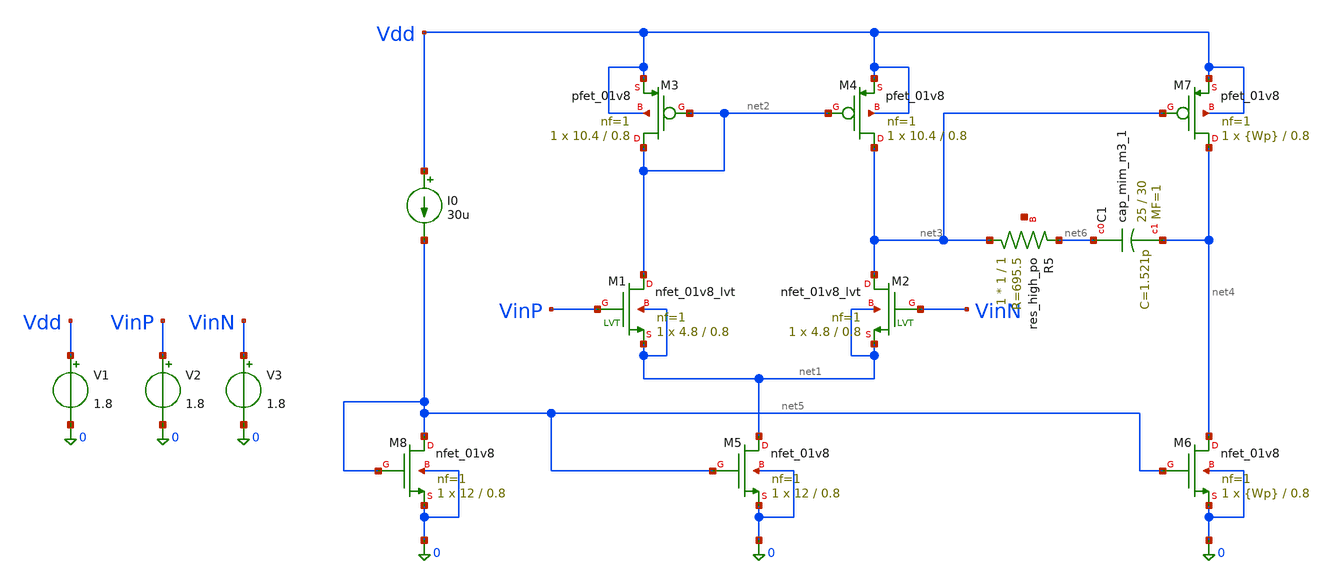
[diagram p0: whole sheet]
** sch_path: parameter_extraction/opamp.sch
**.subckt opamp
XM1 net2 VinP net1 net1 sky130_fd_pr__nfet_01v8_lvt L=0.8 W=4.8 nf=1 ad='int((1 + 1)/2) * 4.8 / 1 * 0.29'
+ as='int((1 + 2)/2) * 4.8 / 1 * 0.29' pd='2*int((1 + 1)/2) * (4.8 / 1 + 0.29)' ps='2*int((1 + 2)/2) * (4.8 / 1 + 0.29)'
+ nrd='0.29 / 4.8 ' nrs='0.29 / 4.8 ' sa=0 sb=0 sd=0 mult=1 m=1
XM3 net2 net2 Vdd Vdd sky130_fd_pr__pfet_01v8 L=0.8 W=10.4 nf=1 ad='int((1 + 1)/2) * 10.4 / 1 * 0.29'
+ as='int((1 + 2)/2) * 10.4 / 1 * 0.29' pd='2*int((1 + 1)/2) * (10.4 / 1 + 0.29)' ps='2*int((1 + 2)/2) * (10.4 / 1 + 0.29)'
+ nrd='0.29 / 10.4 ' nrs='0.29 / 10.4 ' sa=0 sb=0 sd=0 mult=1 m=1
XM5 net1 net5 0 0 sky130_fd_pr__nfet_01v8 L=0.8 W=12 nf=1 ad='int((1 + 1)/2) * 12 / 1 * 0.29' as='int((1 + 2)/2) * 12 / 1 * 0.29'
+ pd='2*int((1 + 1)/2) * (12 / 1 + 0.29)' ps='2*int((1 + 2)/2) * (12 / 1 + 0.29)' nrd='0.29 / 12 ' nrs='0.29 / 12 '
+ sa=0 sb=0 sd=0 mult=1 m=1
XM2 net3 VinN net1 net1 sky130_fd_pr__nfet_01v8_lvt L=0.8 W=4.8 nf=1 ad='int((1 + 1)/2) * 4.8 / 1 * 0.29'
+ as='int((1 + 2)/2) * 4.8 / 1 * 0.29' pd='2*int((1 + 1)/2) * (4.8 / 1 + 0.29)' ps='2*int((1 + 2)/2) * (4.8 / 1 + 0.29)'
+ nrd='0.29 / 4.8 ' nrs='0.29 / 4.8 ' sa=0 sb=0 sd=0 mult=1 m=1
XM4 net3 net2 Vdd Vdd sky130_fd_pr__pfet_01v8 L=0.8 W=10.4 nf=1 ad='int((1 + 1)/2) * 10.4 / 1 * 0.29'
+ as='int((1 + 2)/2) * 10.4 / 1 * 0.29' pd='2*int((1 + 1)/2) * (10.4 / 1 + 0.29)' ps='2*int((1 + 2)/2) * (10.4 / 1 + 0.29)'
+ nrd='0.29 / 10.4 ' nrs='0.29 / 10.4 ' sa=0 sb=0 sd=0 mult=1 m=1
XM6 net4 net5 0 0 sky130_fd_pr__nfet_01v8 L=0.8 W={Wp} nf=1 ad='int((1 + 1)/2) * {Wp} / 1 * 0.29' as='int((1 + 2)/2) * {Wp} / 1 * 0.29'
+ pd='2*int((1 + 1)/2) * ({Wp} / 1 + 0.29)' ps='2*int((1 + 2)/2) * ({Wp} / 1 + 0.29)' nrd='0.29 / {Wp} '
+ nrs='0.29 / {Wp} ' sa=0 sb=0 sd=0 mult=1 m=1
XM7 net4 net3 Vdd Vdd sky130_fd_pr__pfet_01v8 L=0.8 W={Wp} nf=1 ad='int((1 + 1)/2) * {Wp} / 1 * 0.29'
+ as='int((1 + 2)/2) * {Wp} / 1 * 0.29' pd='2*int((1 + 1)/2) * ({Wp} / 1 + 0.29)' ps='2*int((1 + 2)/2) * ({Wp} / 1 + 0.29)'
+ nrd='0.29 / {Wp} ' nrs='0.29 / {Wp} ' sa=0 sb=0 sd=0 mult=1 m=1
XC1 net6 net4 sky130_fd_pr__cap_mim_m3_1 W=25 L=30 MF=1 m=1
XM8 net5 net5 0 0 sky130_fd_pr__nfet_01v8 L=0.8 W=12 nf=1 ad='int((1 + 1)/2) * 12 / 1 * 0.29' as='int((1 + 2)/2) * 12 / 1 * 0.29'
+ pd='2*int((1 + 1)/2) * (12 / 1 + 0.29)' ps='2*int((1 + 2)/2) * (12 / 1 + 0.29)' nrd='0.29 / 12 ' nrs='0.29 / 12 '
+ sa=0 sb=0 sd=0 mult=1 m=1
V1 Vdd 0 1.8
I0 Vdd net5 30u
V2 VinP 0 1.8
V3 VinN 0 1.8
XR5 net3 net6 net7 sky130_fd_pr__res_high_po W=1 L=1 mult=1 m=1
**.ends
.end
